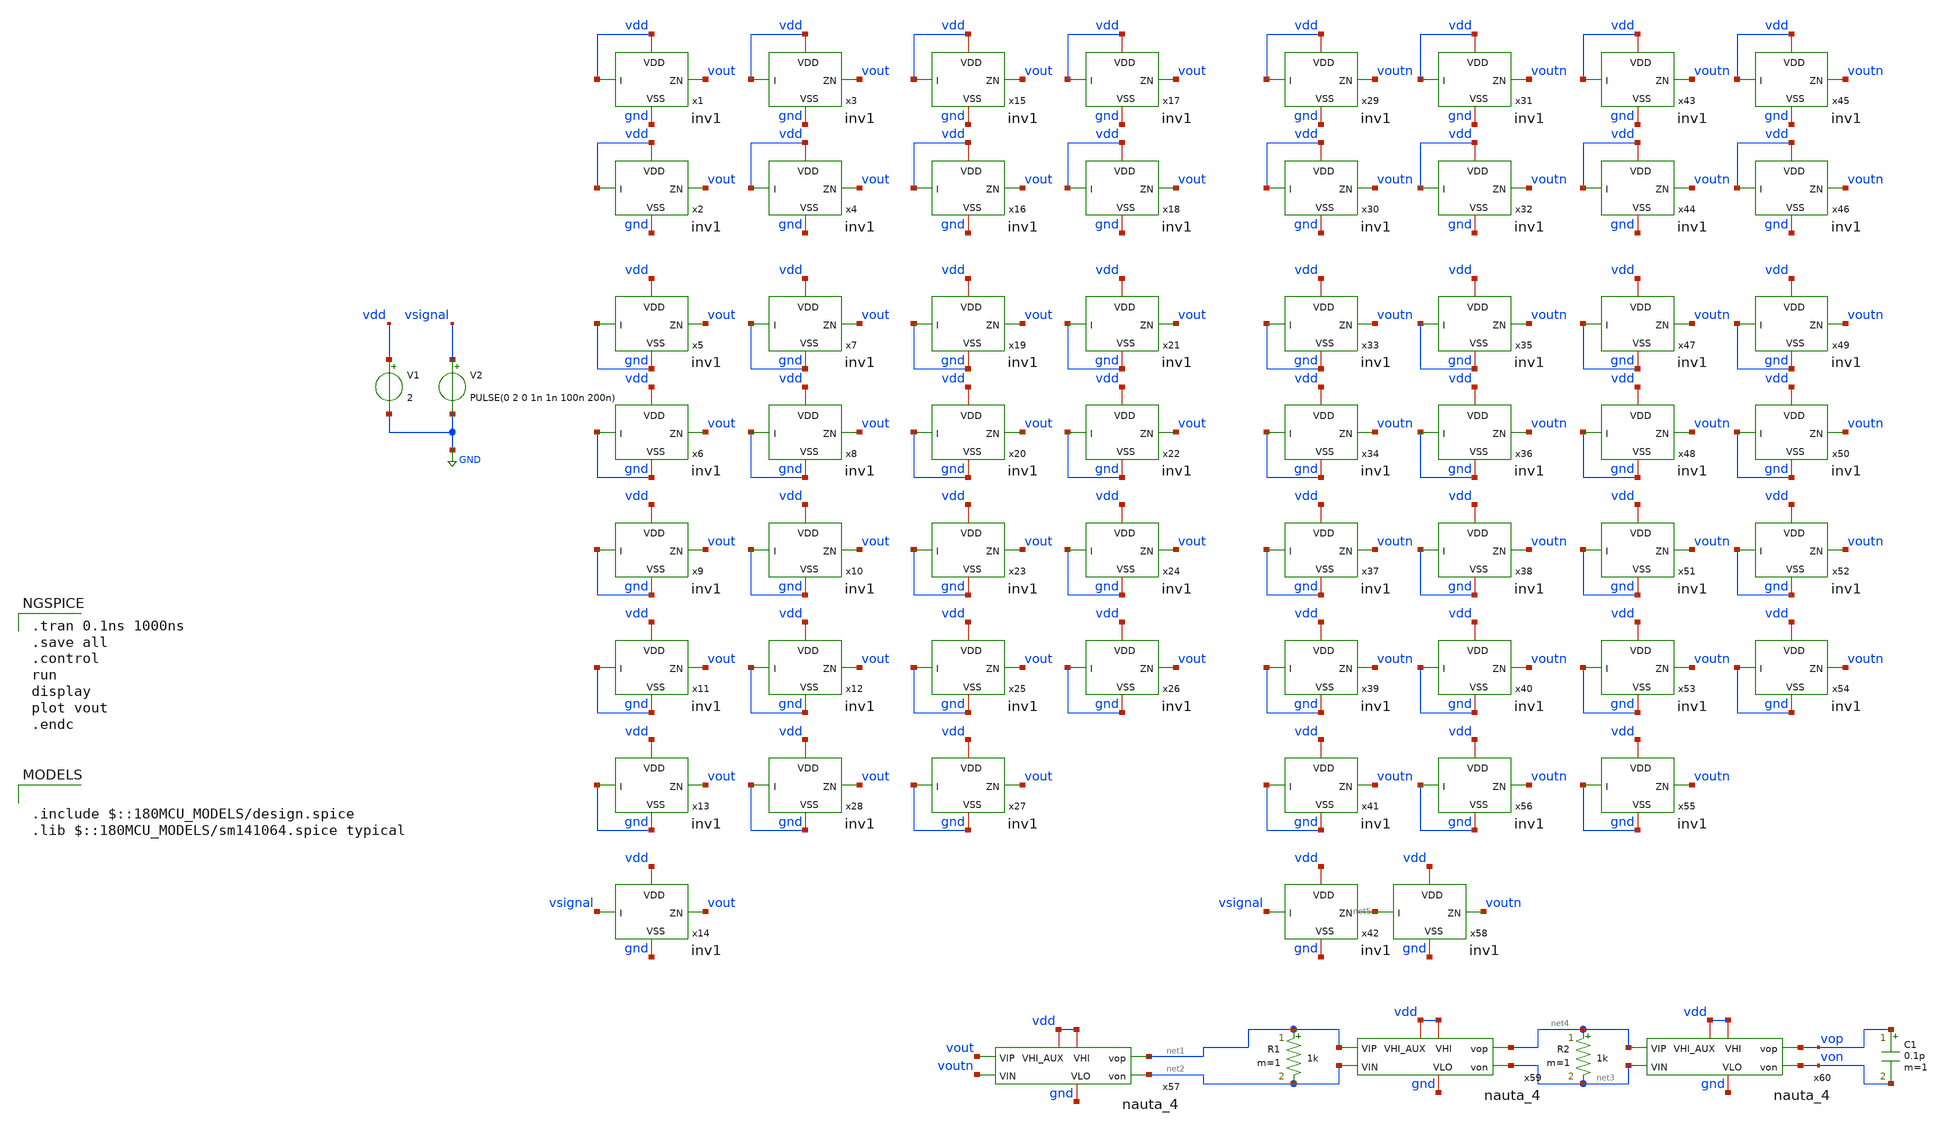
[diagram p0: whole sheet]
** sch_path: xschem/pulse_gen.sch
**.subckt pulse_gen
V1 vdd GND 2
V2 vsignal GND PULSE(0 2 0 1n 1n 100n 200n)
x1 vdd vout vdd gnd inv1
x2 vdd vout vdd gnd inv1
x3 vdd vout vdd gnd inv1
x4 vdd vout vdd gnd inv1
x5 gnd vout vdd gnd inv1
x6 gnd vout vdd gnd inv1
x7 gnd vout vdd gnd inv1
x8 gnd vout vdd gnd inv1
x9 gnd vout vdd gnd inv1
x10 gnd vout vdd gnd inv1
x11 gnd vout vdd gnd inv1
x12 gnd vout vdd gnd inv1
x13 gnd vout vdd gnd inv1
x14 vsignal vout vdd gnd inv1
x15 vdd vout vdd gnd inv1
x16 vdd vout vdd gnd inv1
x17 vdd vout vdd gnd inv1
x18 vdd vout vdd gnd inv1
x19 gnd vout vdd gnd inv1
x20 gnd vout vdd gnd inv1
x21 gnd vout vdd gnd inv1
x22 gnd vout vdd gnd inv1
x23 gnd vout vdd gnd inv1
x24 gnd vout vdd gnd inv1
x25 gnd vout vdd gnd inv1
x26 gnd vout vdd gnd inv1
x27 gnd vout vdd gnd inv1
x28 gnd vout vdd gnd inv1
x29 vdd voutn vdd gnd inv1
x30 vdd voutn vdd gnd inv1
x31 vdd voutn vdd gnd inv1
x32 vdd voutn vdd gnd inv1
x33 gnd voutn vdd gnd inv1
x34 gnd voutn vdd gnd inv1
x35 gnd voutn vdd gnd inv1
x36 gnd voutn vdd gnd inv1
x37 gnd voutn vdd gnd inv1
x38 gnd voutn vdd gnd inv1
x39 gnd voutn vdd gnd inv1
x40 gnd voutn vdd gnd inv1
x41 gnd voutn vdd gnd inv1
x42 vsignal net5 vdd gnd inv1
x43 vdd voutn vdd gnd inv1
x44 vdd voutn vdd gnd inv1
x45 vdd voutn vdd gnd inv1
x46 vdd voutn vdd gnd inv1
x47 gnd voutn vdd gnd inv1
x48 gnd voutn vdd gnd inv1
x49 gnd voutn vdd gnd inv1
x50 gnd voutn vdd gnd inv1
x51 gnd voutn vdd gnd inv1
x52 gnd voutn vdd gnd inv1
x53 gnd voutn vdd gnd inv1
x54 gnd voutn vdd gnd inv1
x55 gnd voutn vdd gnd inv1
x56 gnd voutn vdd gnd inv1
x57 vdd vdd vout net1 voutn net2 gnd nauta_4
R1 net1 net2 1k m=1
x58 net5 voutn vdd gnd inv1
x59 vdd vdd net1 net4 net2 net3 gnd nauta_4
R2 net4 net3 1k m=1
x60 vdd vdd net4 vop net3 von gnd nauta_4
C1 vop von 0.1p m=1
**** begin user architecture code

.include $::180MCU_MODELS/design.spice
.lib $::180MCU_MODELS/sm141064.spice typical


.tran 0.1ns 1000ns
.save all
.control
run
display
plot vout
.endc


**** end user architecture code
**.ends

* expanding   symbol:  inv1.sym # of pins=4
** sym_path: xschem/inv1.sym
** sch_path: xschem/inv1.sch
.subckt inv1 I ZN VDD VSS
*.ipin I
*.iopin VDD
*.iopin VSS
*.opin ZN
**** begin user architecture code

.subckt A ZN I VSS VDD
X0 ZN I VSS VSS nmos_6p0 w=0.82u l=0.6u
X1 ZN I VDD VDD pmos_6p0 w=1.22u l=0.5u
.ends
XDUT ZN I VSS VDD A


**** end user architecture code
.ends


* expanding   symbol:  nauta_4.sym # of pins=7
** sym_path: xschem/nauta_4.sym
** sch_path: xschem/nauta_4.sch
.subckt nauta_4 VHI_AUX VHI VIP vop VIN von VLO
*.ipin VIP
*.ipin VIN
*.opin vop
*.opin von
*.iopin VHI
*.iopin VHI_AUX
*.iopin VLO
**** begin user architecture code

.subckt NAUTA VOP VON VIP VIN VHI VHI_AUX VLO

XA0N VON VIP VLO VLO nmos_6p0 w=0.82u l=0.6u
XA0P VON VIP VHI VHI pmos_6p0 w=1.22u l=0.5u
XA1N VON VIP VLO VLO nmos_6p0 w=0.82u l=0.6u
XA1P VON VIP VHI VHI pmos_6p0 w=1.22u l=0.5u

XB0N VOP VIN VLO VLO nmos_6p0 w=0.82u l=0.6u
XB0P VOP VIN VHI VHI pmos_6p0 w=1.22u l=0.5u
XB1N VOP VIN VLO VLO nmos_6p0 w=0.82u l=0.6u
XB1P VOP VIN VHI VHI pmos_6p0 w=1.22u l=0.5u

XC0N VOP VON VLO VLO nmos_6p0 w=0.82u l=0.6u
XC0P VOP VON VHI VHI pmos_6p0 w=1.22u l=0.5u

XD0N VON VOP VLO VLO nmos_6p0 w=0.82u l=0.6u
XD0P VON VOP VHI VHI pmos_6p0 w=1.22u l=0.5u

XC1N VOP VOP VLO VLO nmos_6p0 w=0.82u l=0.6u
XC1P VOP VOP VHI_AUX VHI_AUX pmos_6p0 w=1.22u l=0.5u

XD1N VON VON VLO VLO nmos_6p0 w=0.82u l=0.6u
XD1P VON VON VHI_AUX VHI_AUX pmos_6p0 w=1.22u l=0.5u

.ends

XDUT VOP VON VIP VIN VHI VHI_AUX VLO NAUTA


**** end user architecture code
.ends

.GLOBAL GND
.end
